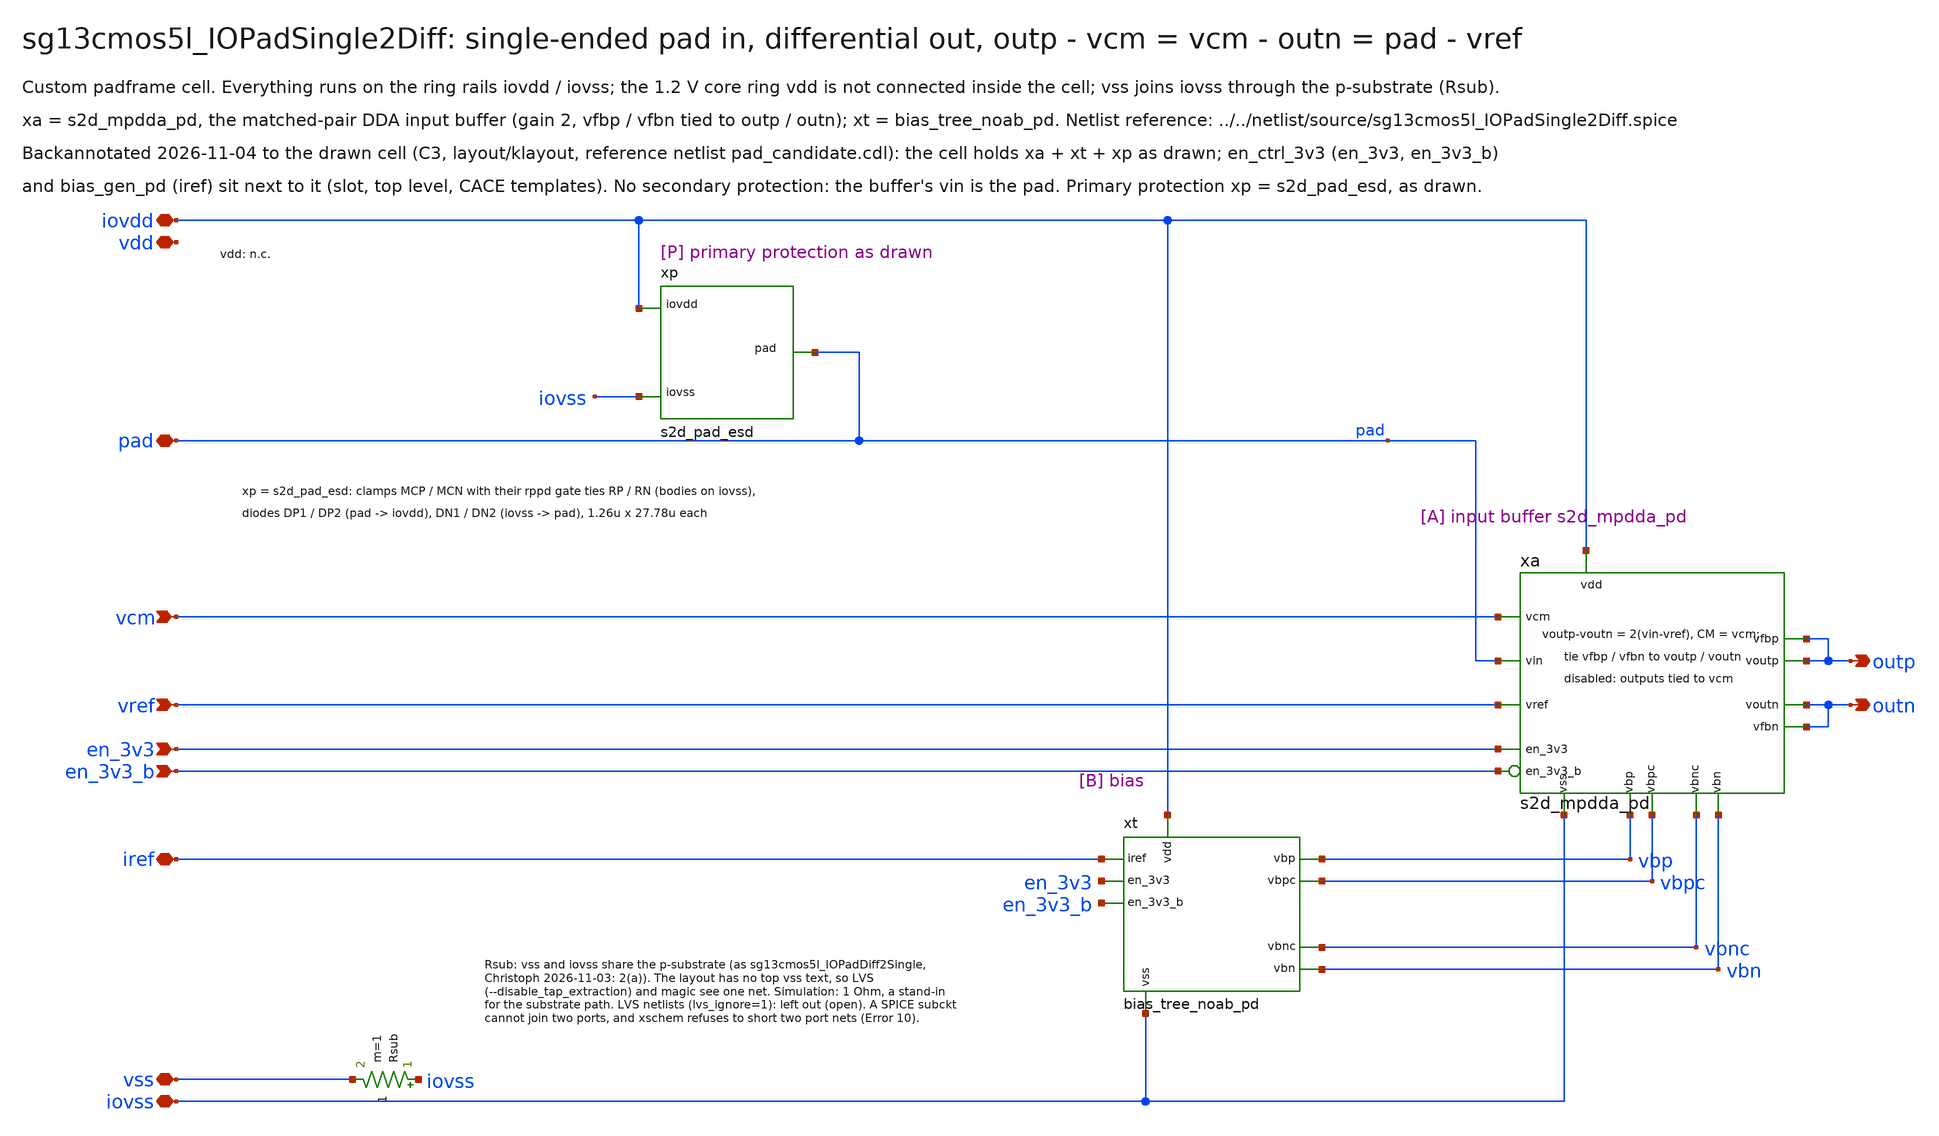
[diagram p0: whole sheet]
** sch_path: macros/sg13cmos5l_IOPadSingle2Diff/schematic/xschem/sg13cmos5l_IOPadSingle2Diff.sch
**.subckt sg13cmos5l_IOPadSingle2Diff iovdd iovss vdd vss pad outp outn vcm vref iref en_3v3
*+ en_3v3_b
*.iopin iovdd
*.iopin iovss
*.iopin vdd
*.iopin vss
*.iopin pad
*.opin outp
*.opin outn
*.ipin vcm
*.ipin vref
*.iopin iref
*.ipin en_3v3
*.ipin en_3v3_b
xt iovdd iovss iref vbp vbn vbpc vbnc en_3v3 en_3v3_b bias_tree_noab_pd
xa iovdd iovss pad vref vcm outp outn outp outn vbp vbn vbpc vbnc en_3v3 en_3v3_b s2d_mpdda_pd
xp iovdd iovss pad s2d_pad_esd
Rsub iovss vss 1 m=1
**.ends
.end
